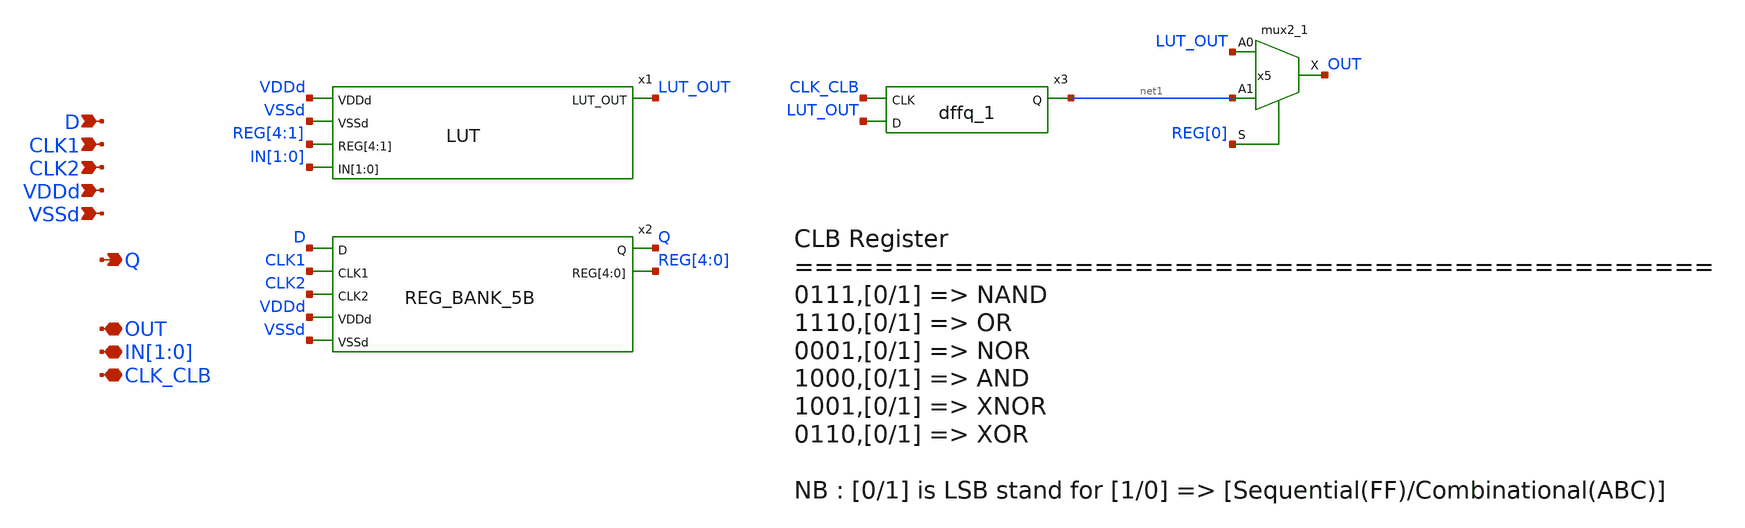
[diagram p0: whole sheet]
** sch_path: designs/libs/core_fpga/clb_2bit/clb_2bit_sc.sch
**.subckt clb_2bit_sc VDDd VSSd D CLK1 CLK2 Q OUT IN[1],IN[0] CLK_CLB
*.ipin VDDd
*.ipin VSSd
*.ipin D
*.ipin CLK1
*.ipin CLK2
*.opin Q
*.iopin OUT
*.iopin IN[1],IN[0]
*.iopin CLK_CLB
x3 CLK_CLB LUT_OUT VDD VNW VPW VSS gf180mcu_fd_sc_mcu9t5v0__dffq_1
x5 LUT_OUT net1 REG[0] VSSd VDDd VSSd VDDd OUT gf180mcu_fd_sc_mcu9t5v0__mux2_1
x1 VDDd VSSd REG[4] REG[3] REG[2] REG[1] IN[1] IN[0] LUT_OUT LUT
x2 D CLK1 CLK2 VDDd VSSd Q REG[4] REG[3] REG[2] REG[1] REG[0] REG_BANK_5B
**.ends
.end
